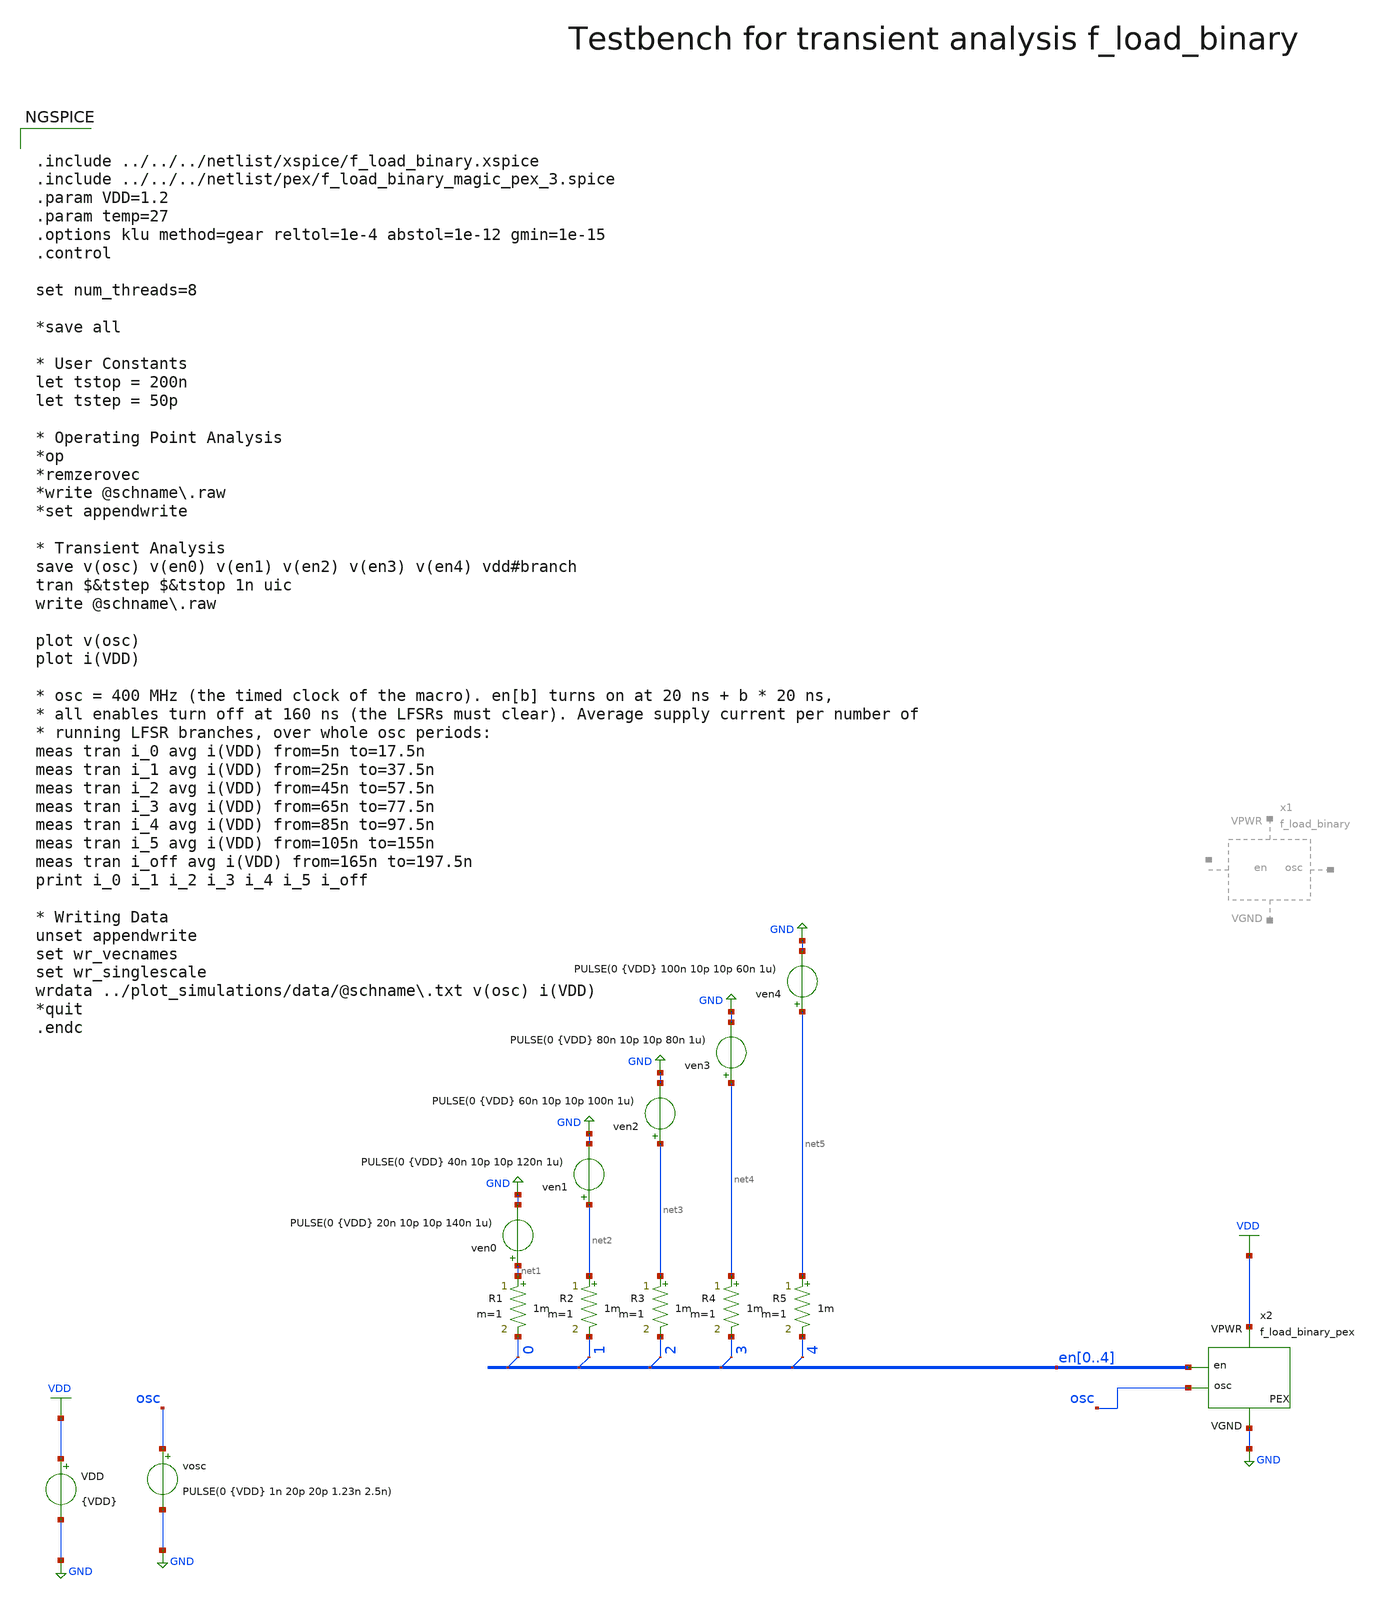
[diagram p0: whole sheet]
** sch_path: macros/heichips26_digital_project/macros/f_load_binary/testbenches/xschem/f_load_binary_tb_tran.sch
**.subckt f_load_binary_tb_tran
VDD VDD GND {VDD}
ven0 net1 GND PULSE(0 {VDD} 20n 10p 10p 140n 1u)
x2 VDD GND en0 en1 en2 en3 en4 osc f_load_binary_pex
* tap: en[0..4] --> en0
* tap: en[0..4] --> en2
* tap: en[0..4] --> en4
* tap: en[0..4] --> en3
* tap: en[0..4] --> en1
vosc osc GND PULSE(0 {VDD} 1n 20p 20p 1.23n 2.5n)
R1 net1 en0 1m m=1
R2 net2 en1 1m m=1
R3 net3 en2 1m m=1
R4 net4 en3 1m m=1
R5 net5 en4 1m m=1
ven1 net2 GND PULSE(0 {VDD} 40n 10p 10p 120n 1u)
ven2 net3 GND PULSE(0 {VDD} 60n 10p 10p 100n 1u)
ven3 net4 GND PULSE(0 {VDD} 80n 10p 10p 80n 1u)
ven4 net5 GND PULSE(0 {VDD} 100n 10p 10p 60n 1u)
**** begin user architecture code


.include ../../../netlist/xspice/f_load_binary.xspice
.include ../../../netlist/pex/f_load_binary_magic_pex_3.spice
.param VDD=1.2
.param temp=27
.options klu method=gear reltol=1e-4 abstol=1e-12 gmin=1e-15
.control

set num_threads=8

*save all

* User Constants
let tstop = 200n
let tstep = 50p

* Operating Point Analysis
*op
*remzerovec
*write @schname\.raw
*set appendwrite

* Transient Analysis
save v(osc) v(en0) v(en1) v(en2) v(en3) v(en4) vdd#branch
tran $&tstep $&tstop 1n uic
write @schname\.raw

plot v(osc)
plot i(VDD)

* osc = 400 MHz (the timed clock of the macro). en[b] turns on at 20 ns + b * 20 ns,
* all enables turn off at 160 ns (the LFSRs must clear). Average supply current per number of
* running LFSR branches, over whole osc periods:
meas tran i_0 avg i(VDD) from=5n to=17.5n
meas tran i_1 avg i(VDD) from=25n to=37.5n
meas tran i_2 avg i(VDD) from=45n to=57.5n
meas tran i_3 avg i(VDD) from=65n to=77.5n
meas tran i_4 avg i(VDD) from=85n to=97.5n
meas tran i_5 avg i(VDD) from=105n to=155n
meas tran i_off avg i(VDD) from=165n to=197.5n
print i_0 i_1 i_2 i_3 i_4 i_5 i_off

* Writing Data
unset appendwrite
set wr_vecnames
set wr_singlescale
wrdata ../plot_simulations/data/@schname\.txt v(osc) i(VDD)
*quit
.endc


.lib cornerMOSlv.lib mos_tt
.lib cornerMOShv.lib mos_tt
.lib cornerRES.lib res_typ
.lib cornerDIO.lib dio_tt

**** end user architecture code
**.ends
.GLOBAL GND
.GLOBAL VDD
.end
